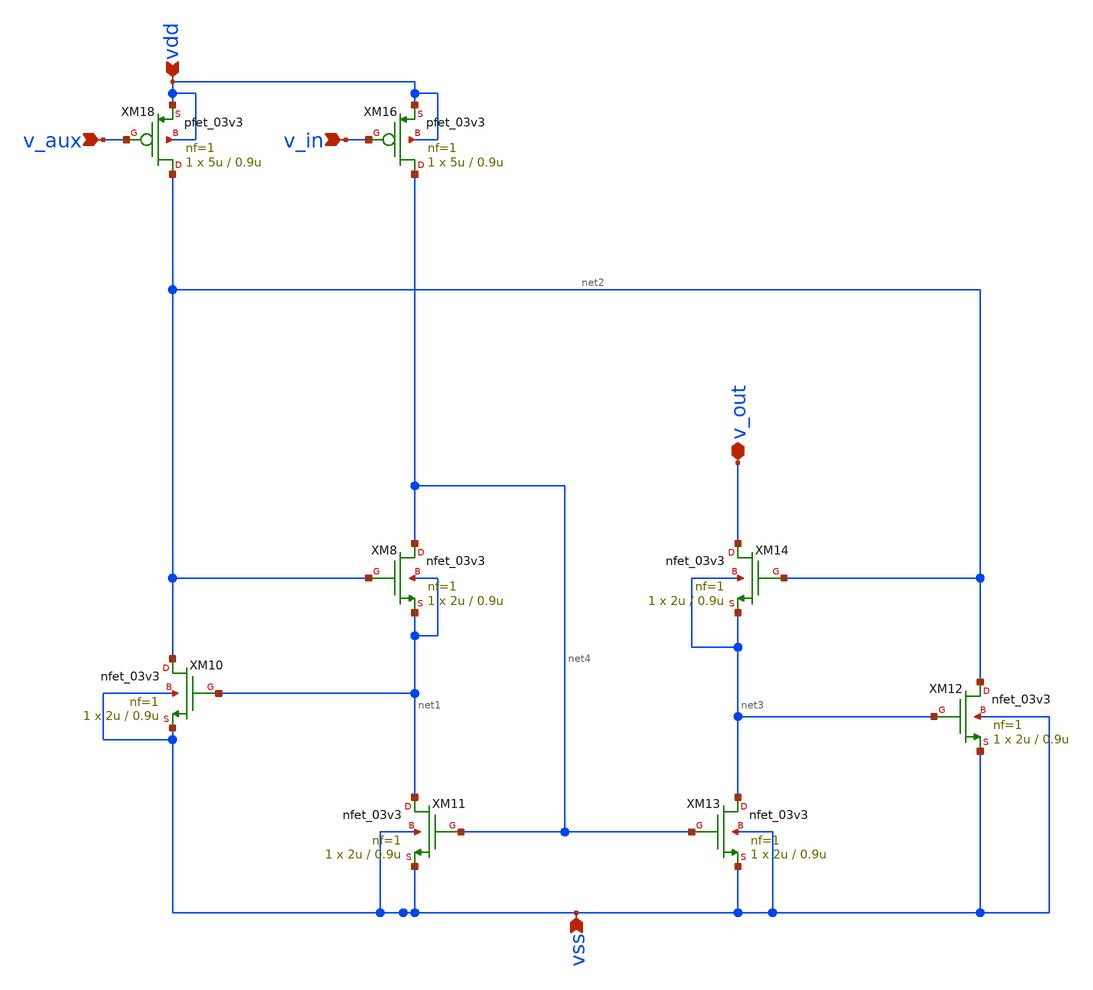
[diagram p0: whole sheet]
** sch_path: blocks/composite/regulated_cascoded_cmirror/xschem/cascode_cm.sch
**.subckt cascode_cm v_in vdd vss v_aux v_out
*.ipin v_in
*.ipin vdd
*.ipin vss
*.ipin v_aux
*.iopin v_out
XM10 net2 net1 vss vss nfet_03v3 L=0.9u W=2u nf=1 ad='int((nf+1)/2) * W/nf * 0.18u' as='int((nf+2)/2) * W/nf * 0.18u'
+ pd='2*int((nf+1)/2) * (W/nf + 0.18u)' ps='2*int((nf+2)/2) * (W/nf + 0.18u)' nrd='0.18u / W' nrs='0.18u / W'
+ sa=0 sb=0 sd=0 m=1
XM8 net4 net2 net1 net1 nfet_03v3 L=0.9u W=2u nf=1 ad='int((nf+1)/2) * W/nf * 0.18u' as='int((nf+2)/2) * W/nf * 0.18u'
+ pd='2*int((nf+1)/2) * (W/nf + 0.18u)' ps='2*int((nf+2)/2) * (W/nf + 0.18u)' nrd='0.18u / W' nrs='0.18u / W'
+ sa=0 sb=0 sd=0 m=1
XM11 net1 net4 vss vss nfet_03v3 L=0.9u W=2u nf=1 ad='int((nf+1)/2) * W/nf * 0.18u' as='int((nf+2)/2) * W/nf * 0.18u'
+ pd='2*int((nf+1)/2) * (W/nf + 0.18u)' ps='2*int((nf+2)/2) * (W/nf + 0.18u)' nrd='0.18u / W' nrs='0.18u / W'
+ sa=0 sb=0 sd=0 m=1
XM12 net2 net3 vss vss nfet_03v3 L=0.9u W=2u nf=1 ad='int((nf+1)/2) * W/nf * 0.18u' as='int((nf+2)/2) * W/nf * 0.18u'
+ pd='2*int((nf+1)/2) * (W/nf + 0.18u)' ps='2*int((nf+2)/2) * (W/nf + 0.18u)' nrd='0.18u / W' nrs='0.18u / W'
+ sa=0 sb=0 sd=0 m=1
XM13 net3 net4 vss vss nfet_03v3 L=0.9u W=2u nf=1 ad='int((nf+1)/2) * W/nf * 0.18u' as='int((nf+2)/2) * W/nf * 0.18u'
+ pd='2*int((nf+1)/2) * (W/nf + 0.18u)' ps='2*int((nf+2)/2) * (W/nf + 0.18u)' nrd='0.18u / W' nrs='0.18u / W'
+ sa=0 sb=0 sd=0 m=1
XM14 v_out net2 net3 net3 nfet_03v3 L=0.9u W=2u nf=1 ad='int((nf+1)/2) * W/nf * 0.18u' as='int((nf+2)/2) * W/nf * 0.18u'
+ pd='2*int((nf+1)/2) * (W/nf + 0.18u)' ps='2*int((nf+2)/2) * (W/nf + 0.18u)' nrd='0.18u / W' nrs='0.18u / W'
+ sa=0 sb=0 sd=0 m=1
XM16 net4 v_in vdd vdd pfet_03v3 L=0.9u W=5u nf=1 ad='int((nf+1)/2) * W/nf * 0.18u' as='int((nf+2)/2) * W/nf * 0.18u'
+ pd='2*int((nf+1)/2) * (W/nf + 0.18u)' ps='2*int((nf+2)/2) * (W/nf + 0.18u)' nrd='0.18u / W' nrs='0.18u / W'
+ sa=0 sb=0 sd=0 m=1
XM18 net2 v_aux vdd vdd pfet_03v3 L=0.9u W=5u nf=1 ad='int((nf+1)/2) * W/nf * 0.18u' as='int((nf+2)/2) * W/nf * 0.18u'
+ pd='2*int((nf+1)/2) * (W/nf + 0.18u)' ps='2*int((nf+2)/2) * (W/nf + 0.18u)' nrd='0.18u / W' nrs='0.18u / W'
+ sa=0 sb=0 sd=0 m=1
**.ends
.end
